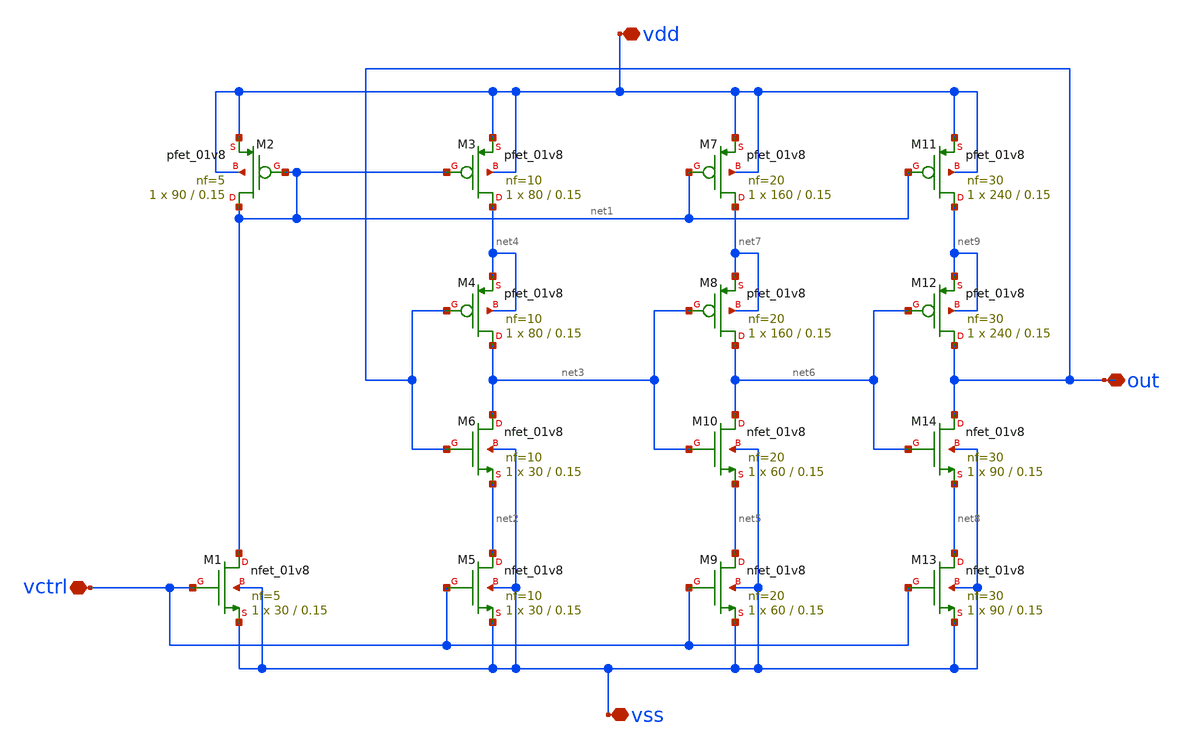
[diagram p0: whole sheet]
** sch_path: xschem/PLL_FOLDER/vco/vco.sch
**.subckt vco vdd vss out vctrl
*.iopin vdd
*.iopin vss
*.iopin out
*.iopin vctrl
XM1 net1 vctrl vss vss sky130_fd_pr__nfet_01v8 L=0.15 W=30 nf=5 ad='int((nf+1)/2) * W/nf * 0.29' as='int((nf+2)/2) * W/nf * 0.29'
+ pd='2*int((nf+1)/2) * (W/nf + 0.29)' ps='2*int((nf+2)/2) * (W/nf + 0.29)' nrd='0.29 / W' nrs='0.29 / W'
+ sa=0 sb=0 sd=0 mult=1 m=1
XM2 net1 net1 vdd vdd sky130_fd_pr__pfet_01v8 L=0.15 W=90 nf=5 ad='int((nf+1)/2) * W/nf * 0.29' as='int((nf+2)/2) * W/nf * 0.29'
+ pd='2*int((nf+1)/2) * (W/nf + 0.29)' ps='2*int((nf+2)/2) * (W/nf + 0.29)' nrd='0.29 / W' nrs='0.29 / W'
+ sa=0 sb=0 sd=0 mult=1 m=1
XM3 net4 net1 vdd vdd sky130_fd_pr__pfet_01v8 L=0.15 W=80 nf=10 ad='int((nf+1)/2) * W/nf * 0.29' as='int((nf+2)/2) * W/nf * 0.29'
+ pd='2*int((nf+1)/2) * (W/nf + 0.29)' ps='2*int((nf+2)/2) * (W/nf + 0.29)' nrd='0.29 / W' nrs='0.29 / W'
+ sa=0 sb=0 sd=0 mult=1 m=1
XM4 net3 out net4 net4 sky130_fd_pr__pfet_01v8 L=0.15 W=80 nf=10 ad='int((nf+1)/2) * W/nf * 0.29' as='int((nf+2)/2) * W/nf * 0.29'
+ pd='2*int((nf+1)/2) * (W/nf + 0.29)' ps='2*int((nf+2)/2) * (W/nf + 0.29)' nrd='0.29 / W' nrs='0.29 / W'
+ sa=0 sb=0 sd=0 mult=1 m=1
XM5 net2 vctrl vss vss sky130_fd_pr__nfet_01v8 L=0.15 W=30 nf=10 ad='int((nf+1)/2) * W/nf * 0.29' as='int((nf+2)/2) * W/nf * 0.29'
+ pd='2*int((nf+1)/2) * (W/nf + 0.29)' ps='2*int((nf+2)/2) * (W/nf + 0.29)' nrd='0.29 / W' nrs='0.29 / W'
+ sa=0 sb=0 sd=0 mult=1 m=1
XM6 net3 out net2 vss sky130_fd_pr__nfet_01v8 L=0.15 W=30 nf=10 ad='int((nf+1)/2) * W/nf * 0.29' as='int((nf+2)/2) * W/nf * 0.29'
+ pd='2*int((nf+1)/2) * (W/nf + 0.29)' ps='2*int((nf+2)/2) * (W/nf + 0.29)' nrd='0.29 / W' nrs='0.29 / W'
+ sa=0 sb=0 sd=0 mult=1 m=1
XM7 net7 net1 vdd vdd sky130_fd_pr__pfet_01v8 L=0.15 W=160 nf=20 ad='int((nf+1)/2) * W/nf * 0.29' as='int((nf+2)/2) * W/nf * 0.29'
+ pd='2*int((nf+1)/2) * (W/nf + 0.29)' ps='2*int((nf+2)/2) * (W/nf + 0.29)' nrd='0.29 / W' nrs='0.29 / W'
+ sa=0 sb=0 sd=0 mult=1 m=1
XM8 net6 net3 net7 net7 sky130_fd_pr__pfet_01v8 L=0.15 W=160 nf=20 ad='int((nf+1)/2) * W/nf * 0.29' as='int((nf+2)/2) * W/nf * 0.29'
+ pd='2*int((nf+1)/2) * (W/nf + 0.29)' ps='2*int((nf+2)/2) * (W/nf + 0.29)' nrd='0.29 / W' nrs='0.29 / W'
+ sa=0 sb=0 sd=0 mult=1 m=1
XM9 net5 vctrl vss vss sky130_fd_pr__nfet_01v8 L=0.15 W=60 nf=20 ad='int((nf+1)/2) * W/nf * 0.29' as='int((nf+2)/2) * W/nf * 0.29'
+ pd='2*int((nf+1)/2) * (W/nf + 0.29)' ps='2*int((nf+2)/2) * (W/nf + 0.29)' nrd='0.29 / W' nrs='0.29 / W'
+ sa=0 sb=0 sd=0 mult=1 m=1
XM10 net6 net3 net5 vss sky130_fd_pr__nfet_01v8 L=0.15 W=60 nf=20 ad='int((nf+1)/2) * W/nf * 0.29' as='int((nf+2)/2) * W/nf * 0.29'
+ pd='2*int((nf+1)/2) * (W/nf + 0.29)' ps='2*int((nf+2)/2) * (W/nf + 0.29)' nrd='0.29 / W' nrs='0.29 / W'
+ sa=0 sb=0 sd=0 mult=1 m=1
XM11 net9 net1 vdd vdd sky130_fd_pr__pfet_01v8 L=0.15 W=240 nf=30 ad='int((nf+1)/2) * W/nf * 0.29' as='int((nf+2)/2) * W/nf * 0.29'
+ pd='2*int((nf+1)/2) * (W/nf + 0.29)' ps='2*int((nf+2)/2) * (W/nf + 0.29)' nrd='0.29 / W' nrs='0.29 / W'
+ sa=0 sb=0 sd=0 mult=1 m=1
XM12 out net6 net9 net9 sky130_fd_pr__pfet_01v8 L=0.15 W=240 nf=30 ad='int((nf+1)/2) * W/nf * 0.29' as='int((nf+2)/2) * W/nf * 0.29'
+ pd='2*int((nf+1)/2) * (W/nf + 0.29)' ps='2*int((nf+2)/2) * (W/nf + 0.29)' nrd='0.29 / W' nrs='0.29 / W'
+ sa=0 sb=0 sd=0 mult=1 m=1
XM13 net8 vctrl vss vss sky130_fd_pr__nfet_01v8 L=0.15 W=90 nf=30 ad='int((nf+1)/2) * W/nf * 0.29' as='int((nf+2)/2) * W/nf * 0.29'
+ pd='2*int((nf+1)/2) * (W/nf + 0.29)' ps='2*int((nf+2)/2) * (W/nf + 0.29)' nrd='0.29 / W' nrs='0.29 / W'
+ sa=0 sb=0 sd=0 mult=1 m=1
XM14 out net6 net8 vss sky130_fd_pr__nfet_01v8 L=0.15 W=90 nf=30 ad='int((nf+1)/2) * W/nf * 0.29' as='int((nf+2)/2) * W/nf * 0.29'
+ pd='2*int((nf+1)/2) * (W/nf + 0.29)' ps='2*int((nf+2)/2) * (W/nf + 0.29)' nrd='0.29 / W' nrs='0.29 / W'
+ sa=0 sb=0 sd=0 mult=1 m=1
**.ends
.end
